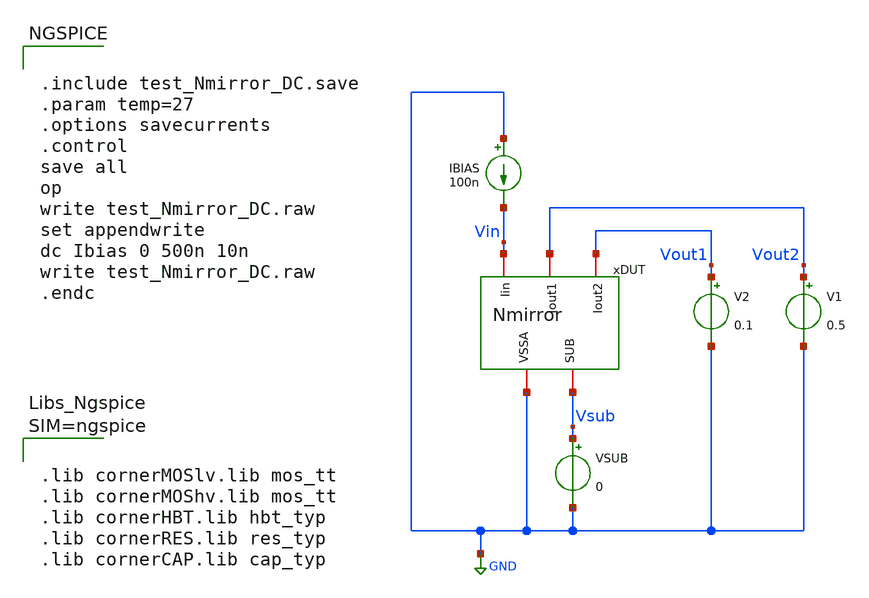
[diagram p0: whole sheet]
** sch_path: xschem/test_Nmirror_DC.sch
**.subckt test_Nmirror_DC
xDUT Vout1 Vin Vout2 GND Vsub Nmirror
IBIAS GND Vin 100n
V1 Vout2 GND 0.5
.save i(v1)
V2 Vout1 GND 0.1
.save i(v2)
VSUB Vsub GND 0
.save i(vsub)
**** begin user architecture code


.include test_Nmirror_DC.save
.param temp=27
.options savecurrents
.control
save all
op
write test_Nmirror_DC.raw
set appendwrite
dc Ibias 0 500n 10n
write test_Nmirror_DC.raw
.endc





.lib cornerMOSlv.lib mos_tt
.lib cornerMOShv.lib mos_tt
.lib cornerHBT.lib hbt_typ
.lib cornerRES.lib res_typ
.lib cornerCAP.lib cap_typ



**** end user architecture code
**.ends
.GLOBAL GND
.end
